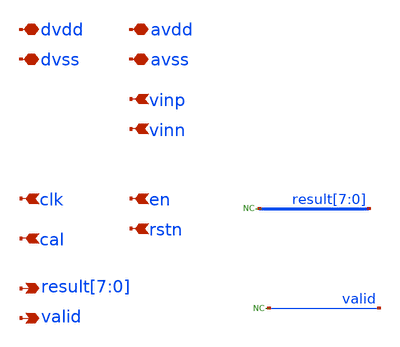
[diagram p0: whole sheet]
** sch_path: post_layout/sar_post.sch
**.subckt sar_post avss avdd dvss dvdd vinp vinn
*+ result[7],result[6],result[5],result[4],result[3],result[2],result[1],result[0] clk en valid cal rstn
*.iopin avss
*.iopin avdd
*.iopin dvss
*.iopin dvdd
*.ipin vinp
*.ipin vinn
*.opin result[7],result[6],result[5],result[4],result[3],result[2],result[1],result[0]
*.ipin clk
*.ipin en
*.opin valid
*.ipin cal
*.ipin rstn
* noconn result[7:0]
* noconn valid
**** begin user architecture code


Xuut dcomp dctln1 dctln0 dctlp1 dctlp0 dctln7 dctln6 dctln5 dctln4 dctln3 dctln2 dtrim4  dtrim1
+ dtrim0 dtrim2 dtrim3 dtrimb3 dtrimb2 dtrimb0 dtrimb1 dtrimb4 dctlp2 dctlp3 dctlp4 dctlp5  dctlp6 dctlp7
+ dclkc dres7 dres6 dres5 dres4 drstn dres3 dres2 dres1 dres0  dvalid dcal den dclk vinp vinn dvdd avdd
+ dvss SAR

.model adc_buff adc_bridge(in_low = 0.2 in_high=0.8)
.model dac_buff dac_bridge(out_high = 1.2)

Aad [clk rstn en comp cal] [dclk drstn den dcomp dcal] adc_buff
Ada [dctlp0 dctlp1 dctlp2 dctlp3 dctlp4 dctlp5 dctlp6 dctlp7 dctln0 dctln1 dctln2 dctln3 dctln4
+ dctln5 dctln6 dctln7 dres0 dres1 dres2 dres3 dres4 dres5 dres6 dres7 dsamp dclkc] [ctlp_0_ ctlp_1_ ctlp_2_
+ ctlp_3_ ctlp_4_ ctlp_5_ ctlp_6_ ctlp_7_ ctln_0_ ctln_1_ ctln_2_ ctln_3_ ctln_4_ ctln_5_ ctln_6_ ctln_7_
+ result_0_ result_1_ result_2_ result_3_ result_4_ result_5_ result_6_ result_7_ sample clkc] dac_buff
Ada2 [dtrim4 dtrim3 dtrim2 dtrim1 dtrim0 dtrimb4 dtrimb3 dtrimb2 dtrimb1 dtrimb0] [trim_4_ trim_3_
+ trim_2_ trim_1_ trim_0_ trimb_4_ trimb_3_ trimb_2_ trimb_1_ trimb_0_ ] dac_buff



**** end user architecture code
**.ends
.end
